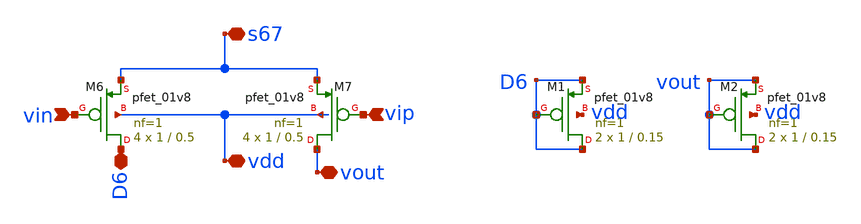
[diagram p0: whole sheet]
** sch_path: opamp/mag/pmosout.sch
**.subckt pmosout vin vip vdd vout s67 D6
*.ipin vin
*.ipin vip
*.iopin vdd
*.iopin vout
*.iopin s67
*.iopin D6
XM6 D6 vin s67 vdd sky130_fd_pr__pfet_01v8 L=0.5 W=1 nf=1 ad='int((nf+1)/2) * W/nf * 0.29' as='int((nf+2)/2) * W/nf * 0.29'
+ pd='2*int((nf+1)/2) * (W/nf + 0.29)' ps='2*int((nf+2)/2) * (W/nf + 0.29)' nrd='0.29 / W' nrs='0.29 / W'
+ sa=0 sb=0 sd=0 mult=4 m=4
XM7 vout vip s67 vdd sky130_fd_pr__pfet_01v8 L=0.5 W=1 nf=1 ad='int((nf+1)/2) * W/nf * 0.29' as='int((nf+2)/2) * W/nf * 0.29'
+ pd='2*int((nf+1)/2) * (W/nf + 0.29)' ps='2*int((nf+2)/2) * (W/nf + 0.29)' nrd='0.29 / W' nrs='0.29 / W'
+ sa=0 sb=0 sd=0 mult=4 m=4
XM1 D6 D6 D6 vdd sky130_fd_pr__pfet_01v8 L=0.15 W=1 nf=1 ad='int((nf+1)/2) * W/nf * 0.29' as='int((nf+2)/2) * W/nf * 0.29'
+ pd='2*int((nf+1)/2) * (W/nf + 0.29)' ps='2*int((nf+2)/2) * (W/nf + 0.29)' nrd='0.29 / W' nrs='0.29 / W'
+ sa=0 sb=0 sd=0 mult=2 m=2
XM2 vout vout vout vdd sky130_fd_pr__pfet_01v8 L=0.15 W=1 nf=1 ad='int((nf+1)/2) * W/nf * 0.29' as='int((nf+2)/2) * W/nf * 0.29'
+ pd='2*int((nf+1)/2) * (W/nf + 0.29)' ps='2*int((nf+2)/2) * (W/nf + 0.29)' nrd='0.29 / W' nrs='0.29 / W'
+ sa=0 sb=0 sd=0 mult=2 m=2
**.ends
.end
